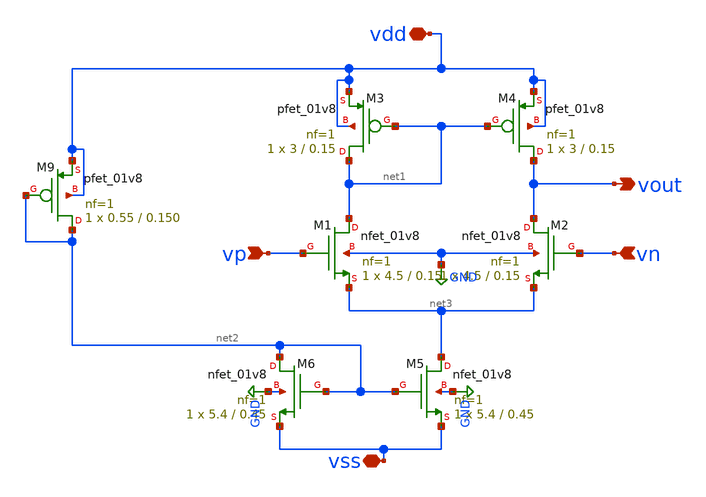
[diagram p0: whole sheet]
** sch_path: designs/subcells/core_ota_1stage/ota_1_stage.sch
**.subckt ota_1_stage vdd vp vout vn vss
*.iopin vdd
*.ipin vp
*.opin vout
*.ipin vn
*.iopin vss
XM1 net1 vp net3 GND sky130_fd_pr__nfet_01v8 L=0.15 W=4.5 nf=1 ad='int((1 + 1)/2) * 4.5 / 1 * 0.29' as='int((1 + 2)/2) * 4.5 / 1 * 0.29'
+ pd='2*int((1 + 1)/2) * (4.5 / 1 + 0.29)' ps='2*int((1 + 2)/2) * (4.5 / 1 + 0.29)' nrd='0.29 / 4.5 ' nrs='0.29 / 4.5 '
+ sa=0 sb=0 sd=0 mult=1 m=1
XM3 net1 net1 vdd vdd sky130_fd_pr__pfet_01v8 L=0.15 W=3 nf=1 ad='int((nf+1)/2) * W/nf * 0.29' as='int((nf+2)/2) * W/nf * 0.29'
+ pd='2*int((nf+1)/2) * (W/nf + 0.29)' ps='2*int((nf+2)/2) * (W/nf + 0.29)' nrd='0.29 / W' nrs='0.29 / W'
+ sa=0 sb=0 sd=0 mult=1 m=1
XM4 vout net1 vdd vdd sky130_fd_pr__pfet_01v8 L=0.15 W=3 nf=1 ad='int((nf+1)/2) * W/nf * 0.29' as='int((nf+2)/2) * W/nf * 0.29'
+ pd='2*int((nf+1)/2) * (W/nf + 0.29)' ps='2*int((nf+2)/2) * (W/nf + 0.29)' nrd='0.29 / W' nrs='0.29 / W'
+ sa=0 sb=0 sd=0 mult=1 m=1
XM2 vout vn net3 GND sky130_fd_pr__nfet_01v8 L=0.15 W=4.5 nf=1 ad='int((1 + 1)/2) * 4.5 / 1 * 0.29' as='int((1 + 2)/2) * 4.5 / 1 * 0.29'
+ pd='2*int((1 + 1)/2) * (4.5 / 1 + 0.29)' ps='2*int((1 + 2)/2) * (4.5 / 1 + 0.29)' nrd='0.29 / 4.5 ' nrs='0.29 / 4.5 '
+ sa=0 sb=0 sd=0 mult=1 m=1
XM5 net3 net2 vss GND sky130_fd_pr__nfet_01v8 L=0.45 W=5.4 nf=1 ad='int((1 + 1)/2) * 5.4 / 1 * 0.29'
+ as='int((1 + 2)/2) * 5.4 / 1 * 0.29' pd='2*int((1 + 1)/2) * (5.4 / 1 + 0.29)' ps='2*int((1 + 2)/2) * (5.4 / 1 + 0.29)'
+ nrd='0.29 / 5.4 ' nrs='0.29 / 5.4 ' sa=0 sb=0 sd=0 mult=1 m=1
XM6 net2 net2 vss GND sky130_fd_pr__nfet_01v8 L=0.45 W=5.4 nf=1 ad='int((1 + 1)/2) * 5.4 / 1 * 0.29'
+ as='int((1 + 2)/2) * 5.4 / 1 * 0.29' pd='2*int((1 + 1)/2) * (5.4 / 1 + 0.29)' ps='2*int((1 + 2)/2) * (5.4 / 1 + 0.29)'
+ nrd='0.29 / 5.4 ' nrs='0.29 / 5.4 ' sa=0 sb=0 sd=0 mult=1 m=1
XM9 net2 net2 vdd vdd sky130_fd_pr__pfet_01v8 L=0.150 W=0.55 nf=1 ad='int((nf+1)/2) * W/nf * 0.29' as='int((nf+2)/2) * W/nf * 0.29'
+ pd='2*int((nf+1)/2) * (W/nf + 0.29)' ps='2*int((nf+2)/2) * (W/nf + 0.29)' nrd='0.29 / W' nrs='0.29 / W'
+ sa=0 sb=0 sd=0 mult=1 m=1
**.ends
.GLOBAL GND
.end
